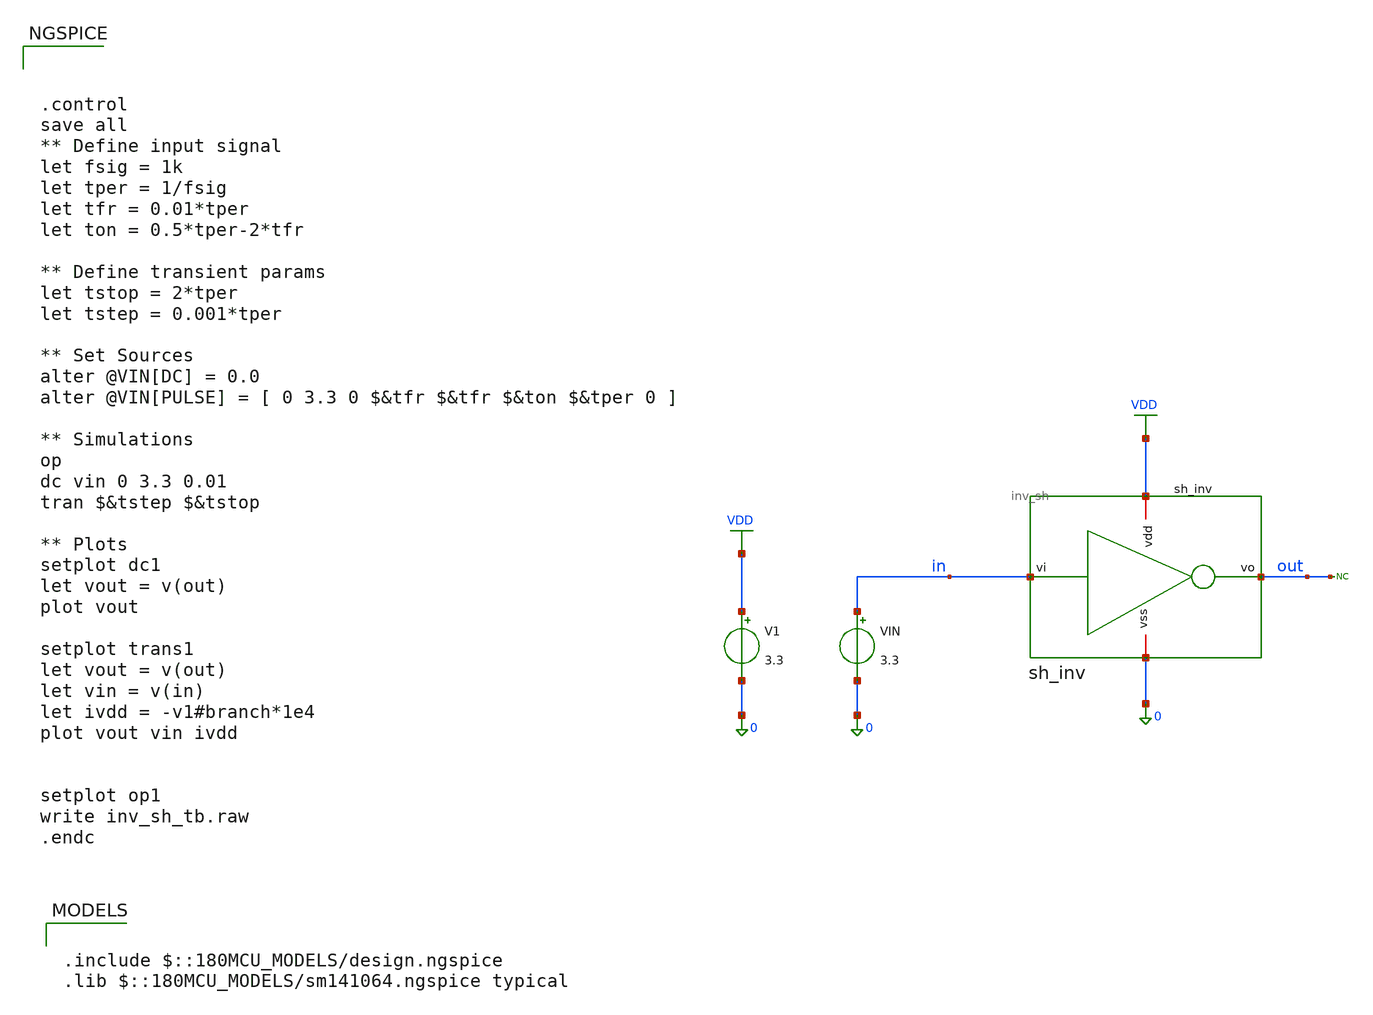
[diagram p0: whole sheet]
** sch_path: xschem/sar_adc/blocks/sample_hold/testbench/inv_sh_tb.sch
**.subckt inv_sh_tb
V1 VDD 0 3.3
VIN in 0 3.3
* noconn out
xinv1 VDD out in 0 inv_sh
**** begin user architecture code

.include $::180MCU_MODELS/design.ngspice
.lib $::180MCU_MODELS/sm141064.ngspice typical




.control
save all
** Define input signal
let fsig = 1k
let tper = 1/fsig
let tfr = 0.01*tper
let ton = 0.5*tper-2*tfr

** Define transient params
let tstop = 2*tper
let tstep = 0.001*tper

** Set Sources
alter @VIN[DC] = 0.0
alter @VIN[PULSE] = [ 0 3.3 0 $&tfr $&tfr $&ton $&tper 0 ]

** Simulations
op
dc vin 0 3.3 0.01
tran $&tstep $&tstop

** Plots
setplot dc1
let vout = v(out)
plot vout

setplot trans1
let vout = v(out)
let vin = v(in)
let ivdd = -v1#branch*1e4
plot vout vin ivdd


setplot op1
write inv_sh_tb.raw
.endc


**** end user architecture code
**.ends

* expanding   symbol:  sar_adc/blocks/sample_hold/inv_sh.sym # of pins=4
** sym_path: xschem/sar_adc/blocks/sample_hold/inv_sh.sym
** sch_path: xschem/sar_adc/blocks/sample_hold/inv_sh.sch
.subckt inv_sh vdd vo vi vss
*.iopin vdd
*.ipin vi
*.opin vo
*.iopin vss
XM1 vo vi vss vss nfet_03v3 L=0.28u W=1u nf=1 ad='int((nf+1)/2) * W/nf * 0.18u' as='int((nf+2)/2) * W/nf * 0.18u'
+ pd='2*int((nf+1)/2) * (W/nf + 0.18u)' ps='2*int((nf+2)/2) * (W/nf + 0.18u)' nrd='0.18u / W' nrs='0.18u / W'
+ sa=0 sb=0 sd=0 m=1
XM2 vo vi vdd vdd pfet_03v3 L=0.28u W=2u nf=1 ad='int((nf+1)/2) * W/nf * 0.18u' as='int((nf+2)/2) * W/nf * 0.18u'
+ pd='2*int((nf+1)/2) * (W/nf + 0.18u)' ps='2*int((nf+2)/2) * (W/nf + 0.18u)' nrd='0.18u / W' nrs='0.18u / W'
+ sa=0 sb=0 sd=0 m=1
.ends

.GLOBAL VDD
.end
